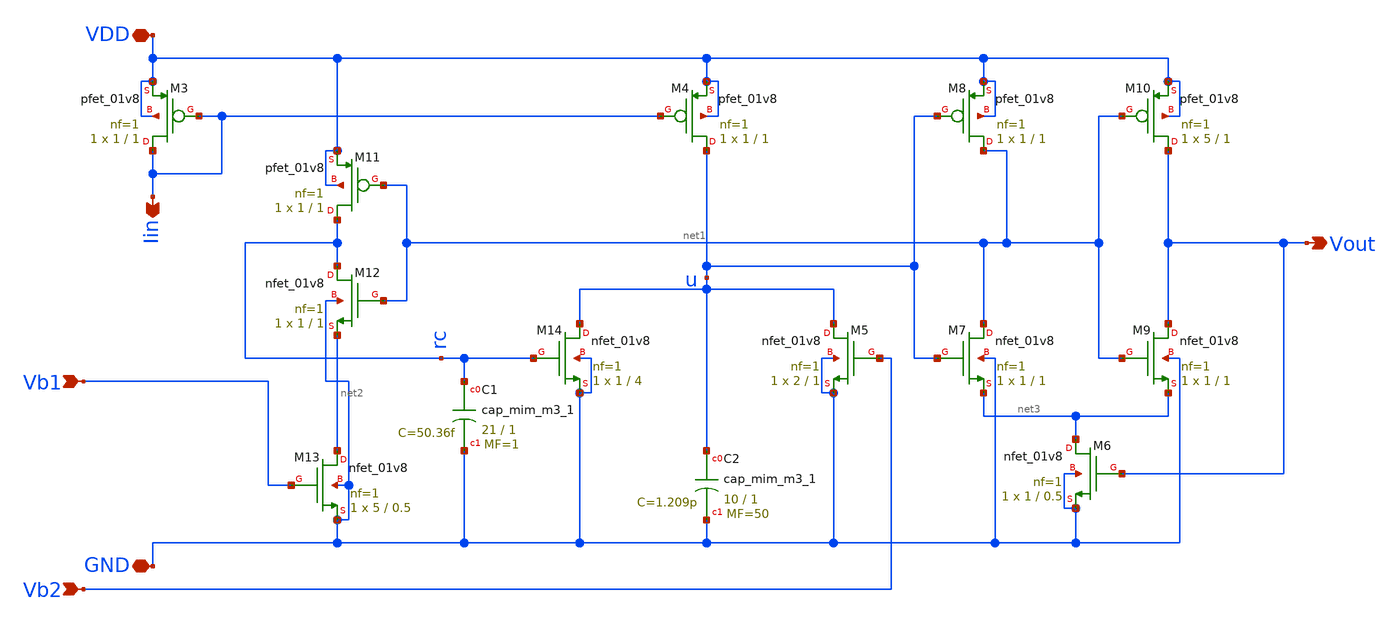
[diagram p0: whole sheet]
** sch_path: LIF_neuron/LIF_neuron_Vohra_v2.sch
**.subckt LIF_neuron_Vohra_v2 Iin GND Vb1 Vb2 VDD Vout
*.opin Iin
*.iopin GND
*.ipin Vb1
*.ipin Vb2
*.iopin VDD
*.opin Vout
XM3 Iin Iin VDD VDD sky130_fd_pr__pfet_01v8 L=1 W=1 nf=1 ad='int((nf+1)/2) * W/nf * 0.29' as='int((nf+2)/2) * W/nf * 0.29'
+ pd='2*int((nf+1)/2) * (W/nf + 0.29)' ps='2*int((nf+2)/2) * (W/nf + 0.29)' nrd='0.29 / W' nrs='0.29 / W'
+ sa=0 sb=0 sd=0 mult=1 m=1
XM13 net2 Vb1 GND GND sky130_fd_pr__nfet_01v8 L=0.5 W=5 nf=1 ad='int((nf+1)/2) * W/nf * 0.29' as='int((nf+2)/2) * W/nf * 0.29'
+ pd='2*int((nf+1)/2) * (W/nf + 0.29)' ps='2*int((nf+2)/2) * (W/nf + 0.29)' nrd='0.29 / W' nrs='0.29 / W'
+ sa=0 sb=0 sd=0 mult=1 m=1
XM12 rc net1 net2 GND sky130_fd_pr__nfet_01v8 L=1 W=1 nf=1 ad='int((nf+1)/2) * W/nf * 0.29' as='int((nf+2)/2) * W/nf * 0.29'
+ pd='2*int((nf+1)/2) * (W/nf + 0.29)' ps='2*int((nf+2)/2) * (W/nf + 0.29)' nrd='0.29 / W' nrs='0.29 / W'
+ sa=0 sb=0 sd=0 mult=1 m=1
XM11 rc net1 VDD VDD sky130_fd_pr__pfet_01v8 L=1 W=1 nf=1 ad='int((nf+1)/2) * W/nf * 0.29' as='int((nf+2)/2) * W/nf * 0.29'
+ pd='2*int((nf+1)/2) * (W/nf + 0.29)' ps='2*int((nf+2)/2) * (W/nf + 0.29)' nrd='0.29 / W' nrs='0.29 / W'
+ sa=0 sb=0 sd=0 mult=1 m=1
XC1 rc GND sky130_fd_pr__cap_mim_m3_1 W=21 L=1 MF=1 m=1
XM14 u rc GND GND sky130_fd_pr__nfet_01v8 L=4 W=1 nf=1 ad='int((nf+1)/2) * W/nf * 0.29' as='int((nf+2)/2) * W/nf * 0.29'
+ pd='2*int((nf+1)/2) * (W/nf + 0.29)' ps='2*int((nf+2)/2) * (W/nf + 0.29)' nrd='0.29 / W' nrs='0.29 / W'
+ sa=0 sb=0 sd=0 mult=1 m=1
XM4 u Iin VDD VDD sky130_fd_pr__pfet_01v8 L=1 W=1 nf=1 ad='int((nf+1)/2) * W/nf * 0.29' as='int((nf+2)/2) * W/nf * 0.29'
+ pd='2*int((nf+1)/2) * (W/nf + 0.29)' ps='2*int((nf+2)/2) * (W/nf + 0.29)' nrd='0.29 / W' nrs='0.29 / W'
+ sa=0 sb=0 sd=0 mult=1 m=1
XC2 u GND sky130_fd_pr__cap_mim_m3_1 W=10 L=1 MF=50 m=50
XM5 u Vb2 GND GND sky130_fd_pr__nfet_01v8 L=1 W=2 nf=1 ad='int((nf+1)/2) * W/nf * 0.29' as='int((nf+2)/2) * W/nf * 0.29'
+ pd='2*int((nf+1)/2) * (W/nf + 0.29)' ps='2*int((nf+2)/2) * (W/nf + 0.29)' nrd='0.29 / W' nrs='0.29 / W'
+ sa=0 sb=0 sd=0 mult=1 m=1
XM6 net3 Vout GND GND sky130_fd_pr__nfet_01v8 L=0.5 W=1 nf=1 ad='int((nf+1)/2) * W/nf * 0.29' as='int((nf+2)/2) * W/nf * 0.29'
+ pd='2*int((nf+1)/2) * (W/nf + 0.29)' ps='2*int((nf+2)/2) * (W/nf + 0.29)' nrd='0.29 / W' nrs='0.29 / W'
+ sa=0 sb=0 sd=0 mult=1 m=1
XM7 net1 u net3 GND sky130_fd_pr__nfet_01v8 L=1 W=1 nf=1 ad='int((nf+1)/2) * W/nf * 0.29' as='int((nf+2)/2) * W/nf * 0.29'
+ pd='2*int((nf+1)/2) * (W/nf + 0.29)' ps='2*int((nf+2)/2) * (W/nf + 0.29)' nrd='0.29 / W' nrs='0.29 / W'
+ sa=0 sb=0 sd=0 mult=1 m=1
XM8 net1 u VDD VDD sky130_fd_pr__pfet_01v8 L=1 W=1 nf=1 ad='int((nf+1)/2) * W/nf * 0.29' as='int((nf+2)/2) * W/nf * 0.29'
+ pd='2*int((nf+1)/2) * (W/nf + 0.29)' ps='2*int((nf+2)/2) * (W/nf + 0.29)' nrd='0.29 / W' nrs='0.29 / W'
+ sa=0 sb=0 sd=0 mult=1 m=1
XM9 Vout net1 net3 GND sky130_fd_pr__nfet_01v8 L=1 W=1 nf=1 ad='int((nf+1)/2) * W/nf * 0.29' as='int((nf+2)/2) * W/nf * 0.29'
+ pd='2*int((nf+1)/2) * (W/nf + 0.29)' ps='2*int((nf+2)/2) * (W/nf + 0.29)' nrd='0.29 / W' nrs='0.29 / W'
+ sa=0 sb=0 sd=0 mult=1 m=1
XM10 Vout net1 VDD VDD sky130_fd_pr__pfet_01v8 L=1 W=5 nf=1 ad='int((nf+1)/2) * W/nf * 0.29' as='int((nf+2)/2) * W/nf * 0.29'
+ pd='2*int((nf+1)/2) * (W/nf + 0.29)' ps='2*int((nf+2)/2) * (W/nf + 0.29)' nrd='0.29 / W' nrs='0.29 / W'
+ sa=0 sb=0 sd=0 mult=1 m=1
**.ends
.end
